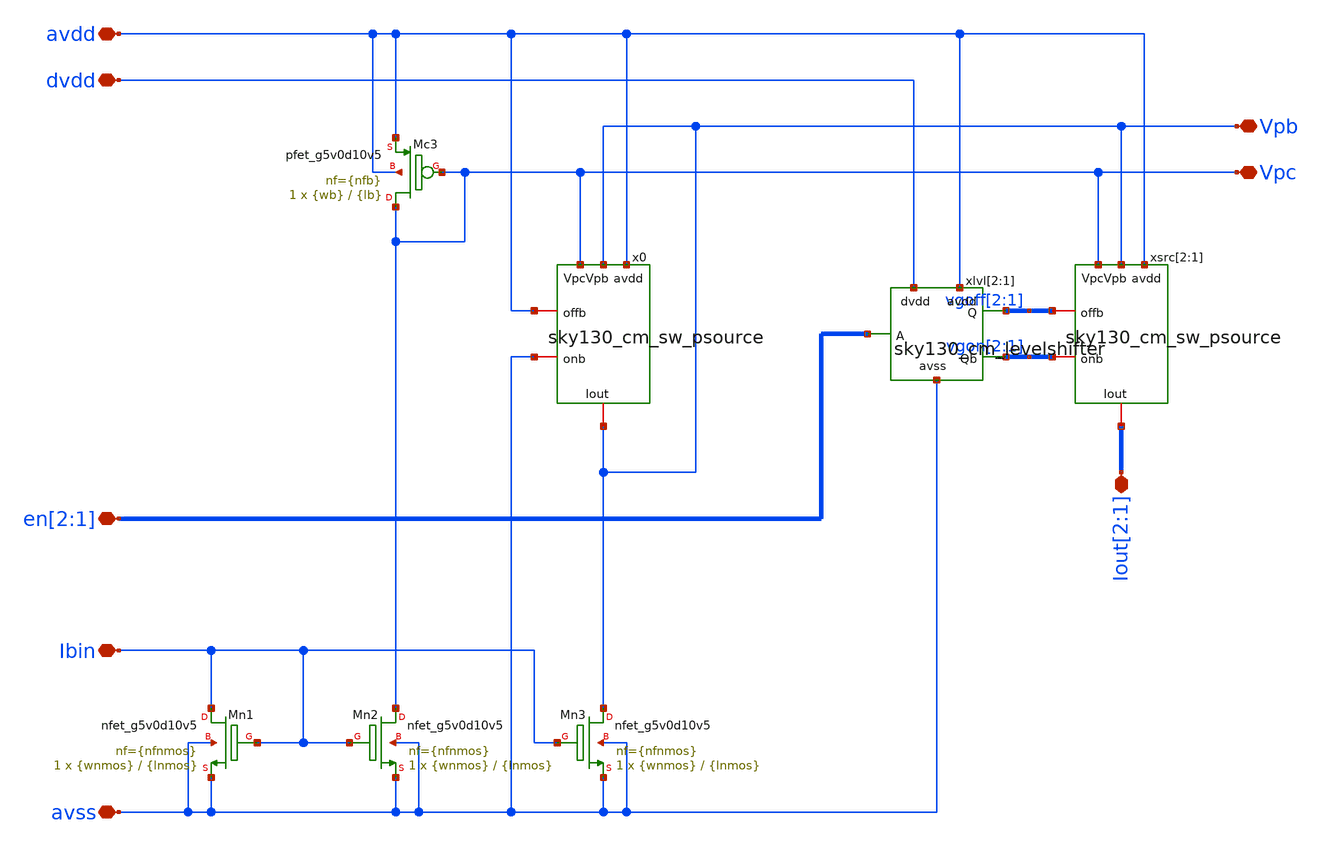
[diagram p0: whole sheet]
** sch_path: xschem/sky130_cm_sources.sch
**.subckt sky130_cm_sources avss avdd Ibin Vpb Vpc Iout[2],Iout[1] dvdd en[2],en[1]
*.iopin avss
*.iopin avdd
*.iopin Ibin
*.iopin Vpb
*.iopin Vpc
*.iopin Iout[2],Iout[1]
*.iopin dvdd
*.iopin en[2],en[1]
XMc3 Vpc Vpc avdd avdd sky130_fd_pr__pfet_g5v0d10v5 L={lb} W={wb} nf={nfb} ad='int(({nfb} + 1)/2) * {wb} / {nfb} * 0.29'
+ as='int(({nfb} + 2)/2) * {wb} / {nfb} * 0.29' pd='2*int(({nfb} + 1)/2) * ({wb} / {nfb} + 0.29)' ps='2*int(({nfb} + 2)/2) * ({wb} / {nfb} + 0.29)'
+ nrd='0.29 / {wb} ' nrs='0.29 / {wb} ' sa=0 sb=0 sd=0 mult=1 m=1
XMn1 Ibin Ibin avss avss sky130_fd_pr__nfet_g5v0d10v5 L={lnmos} W={wnmos} nf={nfnmos} ad='int(({nfnmos} + 1)/2) * {wnmos} / {nfnmos} * 0.29'
+ as='int(({nfnmos} + 2)/2) * {wnmos} / {nfnmos} * 0.29' pd='2*int(({nfnmos} + 1)/2) * ({wnmos} / {nfnmos} + 0.29)'
+ ps='2*int(({nfnmos} + 2)/2) * ({wnmos} / {nfnmos} + 0.29)' nrd='0.29 / {wnmos} ' nrs='0.29 / {wnmos} '
+ sa=0 sb=0 sd=0 mult=1 m=1
XMn2 Vpc Ibin avss avss sky130_fd_pr__nfet_g5v0d10v5 L={lnmos} W={wnmos} nf={nfnmos} ad='int(({nfnmos} + 1)/2) * {wnmos} / {nfnmos} * 0.29'
+ as='int(({nfnmos} + 2)/2) * {wnmos} / {nfnmos} * 0.29' pd='2*int(({nfnmos} + 1)/2) * ({wnmos} / {nfnmos} + 0.29)'
+ ps='2*int(({nfnmos} + 2)/2) * ({wnmos} / {nfnmos} + 0.29)' nrd='0.29 / {wnmos} ' nrs='0.29 / {wnmos} '
+ sa=0 sb=0 sd=0 mult=1 m=1
XMn3 Vpb Ibin avss avss sky130_fd_pr__nfet_g5v0d10v5 L={lnmos} W={wnmos} nf={nfnmos} ad='int(({nfnmos} + 1)/2) * {wnmos} / {nfnmos} * 0.29'
+ as='int(({nfnmos} + 2)/2) * {wnmos} / {nfnmos} * 0.29' pd='2*int(({nfnmos} + 1)/2) * ({wnmos} / {nfnmos} + 0.29)'
+ ps='2*int(({nfnmos} + 2)/2) * ({wnmos} / {nfnmos} + 0.29)' nrd='0.29 / {wnmos} ' nrs='0.29 / {wnmos} '
+ sa=0 sb=0 sd=0 mult=1 m=1
xlvl[2] avdd vgoff[2] dvdd vgon[2] en[2] avss sky130_cm_levelshifter
xlvl[1] avdd vgoff[1] dvdd vgon[1] en[1] avss sky130_cm_levelshifter
x0 avdd avdd Vpb avss Vpc Vpb sky130_cm_sw_psource l={l} w={w} nf={nf} lc={lc} wc={wc} nfc={nfc} lon=.5
+ won=1 nfon=1 loff=.5 woff=1 nfoff=1
xsrc[2] avdd vgoff[2] Vpb vgon[2] Vpc Iout[2] sky130_cm_sw_psource l={l} w={w} nf={nf} lc={lc} wc={wc}
+ nfc={nfc} lon=.5 won=1 nfon=1 loff=.5 woff=1 nfoff=1
xsrc[1] avdd vgoff[1] Vpb vgon[1] Vpc Iout[1] sky130_cm_sw_psource l={l} w={w} nf={nf} lc={lc} wc={wc}
+ nfc={nfc} lon=.5 won=1 nfon=1 loff=.5 woff=1 nfoff=1
**.ends

* expanding   symbol:  xschem/sky130_cm_levelshifter.sym # of pins=6
** sym_path: xschem/sky130_cm_levelshifter.sym
** sch_path: xschem/sky130_cm_levelshifter.sch
.subckt sky130_cm_levelshifter avdd Q dvdd Qb A avss
*.iopin avss
*.iopin avdd
*.iopin A
*.iopin dvdd
*.iopin Qb
*.iopin Q
XMnl1 Q ab avss avss sky130_fd_pr__nfet_g5v0d10v5 L=0.5 W=6 nf=1 ad='int((1 + 1)/2) * 6 / 1 * 0.29' as='int((1 + 2)/2) * 6 / 1 * 0.29'
+ pd='2*int((1 + 1)/2) * (6 / 1 + 0.29)' ps='2*int((1 + 2)/2) * (6 / 1 + 0.29)' nrd='0.29 / 6 ' nrs='0.29 / 6 '
+ sa=0 sb=0 sd=0 mult=1 m=1
XMnl2 Qb abb avss avss sky130_fd_pr__nfet_g5v0d10v5 L=0.5 W=6 nf=1 ad='int((1 + 1)/2) * 6 / 1 * 0.29'
+ as='int((1 + 2)/2) * 6 / 1 * 0.29' pd='2*int((1 + 1)/2) * (6 / 1 + 0.29)' ps='2*int((1 + 2)/2) * (6 / 1 + 0.29)'
+ nrd='0.29 / 6 ' nrs='0.29 / 6 ' sa=0 sb=0 sd=0 mult=1 m=1
XMpl1 Q Qb avdd avdd sky130_fd_pr__pfet_g5v0d10v5 L=0.5 W=2 nf=1 ad='int((1 + 1)/2) * 2 / 1 * 0.29' as='int((1 + 2)/2) * 2 / 1 * 0.29'
+ pd='2*int((1 + 1)/2) * (2 / 1 + 0.29)' ps='2*int((1 + 2)/2) * (2 / 1 + 0.29)' nrd='0.29 / 2 ' nrs='0.29 / 2 '
+ sa=0 sb=0 sd=0 mult=1 m=1
XMpl2 Qb Q avdd avdd sky130_fd_pr__pfet_g5v0d10v5 L=0.5 W=2 nf=1 ad='int((1 + 1)/2) * 2 / 1 * 0.29' as='int((1 + 2)/2) * 2 / 1 * 0.29'
+ pd='2*int((1 + 1)/2) * (2 / 1 + 0.29)' ps='2*int((1 + 2)/2) * (2 / 1 + 0.29)' nrd='0.29 / 2 ' nrs='0.29 / 2 '
+ sa=0 sb=0 sd=0 mult=1 m=1
XMn1 ab A avss avss sky130_fd_pr__nfet_01v8 L=0.15 W=1 nf=1 ad='int((1 + 1)/2) * 1 / 1 * 0.29' as='int((1 + 2)/2) * 1 / 1 * 0.29'
+ pd='2*int((1 + 1)/2) * (1 / 1 + 0.29)' ps='2*int((1 + 2)/2) * (1 / 1 + 0.29)' nrd='0.29 / 1 ' nrs='0.29 / 1 '
+ sa=0 sb=0 sd=0 mult=1 m=1
XMp1 ab A dvdd dvdd sky130_fd_pr__pfet_01v8 L=0.15 W=2 nf=1 ad='int((nf+1)/2) * W/nf * 0.29' as='int((nf+2)/2) * W/nf * 0.29'
+ pd='2*int((nf+1)/2) * (W/nf + 0.29)' ps='2*int((nf+2)/2) * (W/nf + 0.29)' nrd='0.29 / W' nrs='0.29 / W'
+ sa=0 sb=0 sd=0 mult=1 m=1
XMn2 abb ab avss avss sky130_fd_pr__nfet_01v8 L=0.15 W=1 nf=1 ad='int((1 + 1)/2) * 1 / 1 * 0.29' as='int((1 + 2)/2) * 1 / 1 * 0.29'
+ pd='2*int((1 + 1)/2) * (1 / 1 + 0.29)' ps='2*int((1 + 2)/2) * (1 / 1 + 0.29)' nrd='0.29 / 1 ' nrs='0.29 / 1 '
+ sa=0 sb=0 sd=0 mult=1 m=1
XMp2 abb ab dvdd dvdd sky130_fd_pr__pfet_01v8 L=0.15 W=2 nf=1 ad='int((nf+1)/2) * W/nf * 0.29' as='int((nf+2)/2) * W/nf * 0.29'
+ pd='2*int((nf+1)/2) * (W/nf + 0.29)' ps='2*int((nf+2)/2) * (W/nf + 0.29)' nrd='0.29 / W' nrs='0.29 / W'
+ sa=0 sb=0 sd=0 mult=1 m=1
.ends


* expanding   symbol:  xschem/sky130_cm_sw_psource.sym # of pins=6
** sym_path: xschem/sky130_cm_sw_psource.sym
** sch_path: xschem/sky130_cm_sw_psource.sch
.subckt sky130_cm_sw_psource avdd offb Vpb onb Vpc Iout  l=8 w=2 nf=1 lc=0.5 wc=2 nfc=1 lon=.5 won=1
+ nfon=1 loff=.5 woff=1 nfoff=1
*.iopin avdd
*.iopin Vpb
*.iopin Vpc
*.iopin Iout
*.iopin offb
*.iopin onb
XMc2 Iout vsw vd avdd sky130_fd_pr__pfet_g5v0d10v5 L={lc} W={wc} nf={nfc} ad='int(({nfc} + 1)/2) * {wc} / {nfc} * 0.29'
+ as='int(({nfc} + 2)/2) * {wc} / {nfc} * 0.29' pd='2*int(({nfc} + 1)/2) * ({wc} / {nfc} + 0.29)' ps='2*int(({nfc} + 2)/2) * ({wc} / {nfc} + 0.29)'
+ nrd='0.29 / {wc} ' nrs='0.29 / {wc} ' sa=0 sb=0 sd=0 mult=1 m=1
XM2 vd Vpb avdd avdd sky130_fd_pr__pfet_g5v0d10v5 L={l} W={w} nf={nf} ad='int(({nf} + 1)/2) * {w} / {nf} * 0.29'
+ as='int(({nf} + 2)/2) * {w} / {nf} * 0.29' pd='2*int(({nf} + 1)/2) * ({w} / {nf} + 0.29)' ps='2*int(({nf} + 2)/2) * ({w} / {nf} + 0.29)'
+ nrd='0.29 / {w} ' nrs='0.29 / {w} ' sa=0 sb=0 sd=0 mult=1 m=1
XMon Vpc onb vsw avdd sky130_fd_pr__pfet_g5v0d10v5 L={lon} W={won} nf={nfon} ad='int(({nfon} + 1)/2) * {won} / {nfon} * 0.29'
+ as='int(({nfon} + 2)/2) * {won} / {nfon} * 0.29' pd='2*int(({nfon} + 1)/2) * ({won} / {nfon} + 0.29)'
+ ps='2*int(({nfon} + 2)/2) * ({won} / {nfon} + 0.29)' nrd='0.29 / {won} ' nrs='0.29 / {won} ' sa=0 sb=0
+ sd=0 mult=1 m=1
XMoff vsw offb avdd avdd sky130_fd_pr__pfet_g5v0d10v5 L={loff} W={woff} nf={nfoff} ad='int(({nfoff} + 1)/2) * {woff} / {nfoff} * 0.29'
+ as='int(({nfoff} + 2)/2) * {woff} / {nfoff} * 0.29' pd='2*int(({nfoff} + 1)/2) * ({woff} / {nfoff} + 0.29)'
+ ps='2*int(({nfoff} + 2)/2) * ({woff} / {nfoff} + 0.29)' nrd='0.29 / {woff} ' nrs='0.29 / {woff} ' sa=0
+ sb=0 sd=0 mult=1 m=1
.ends

.end
